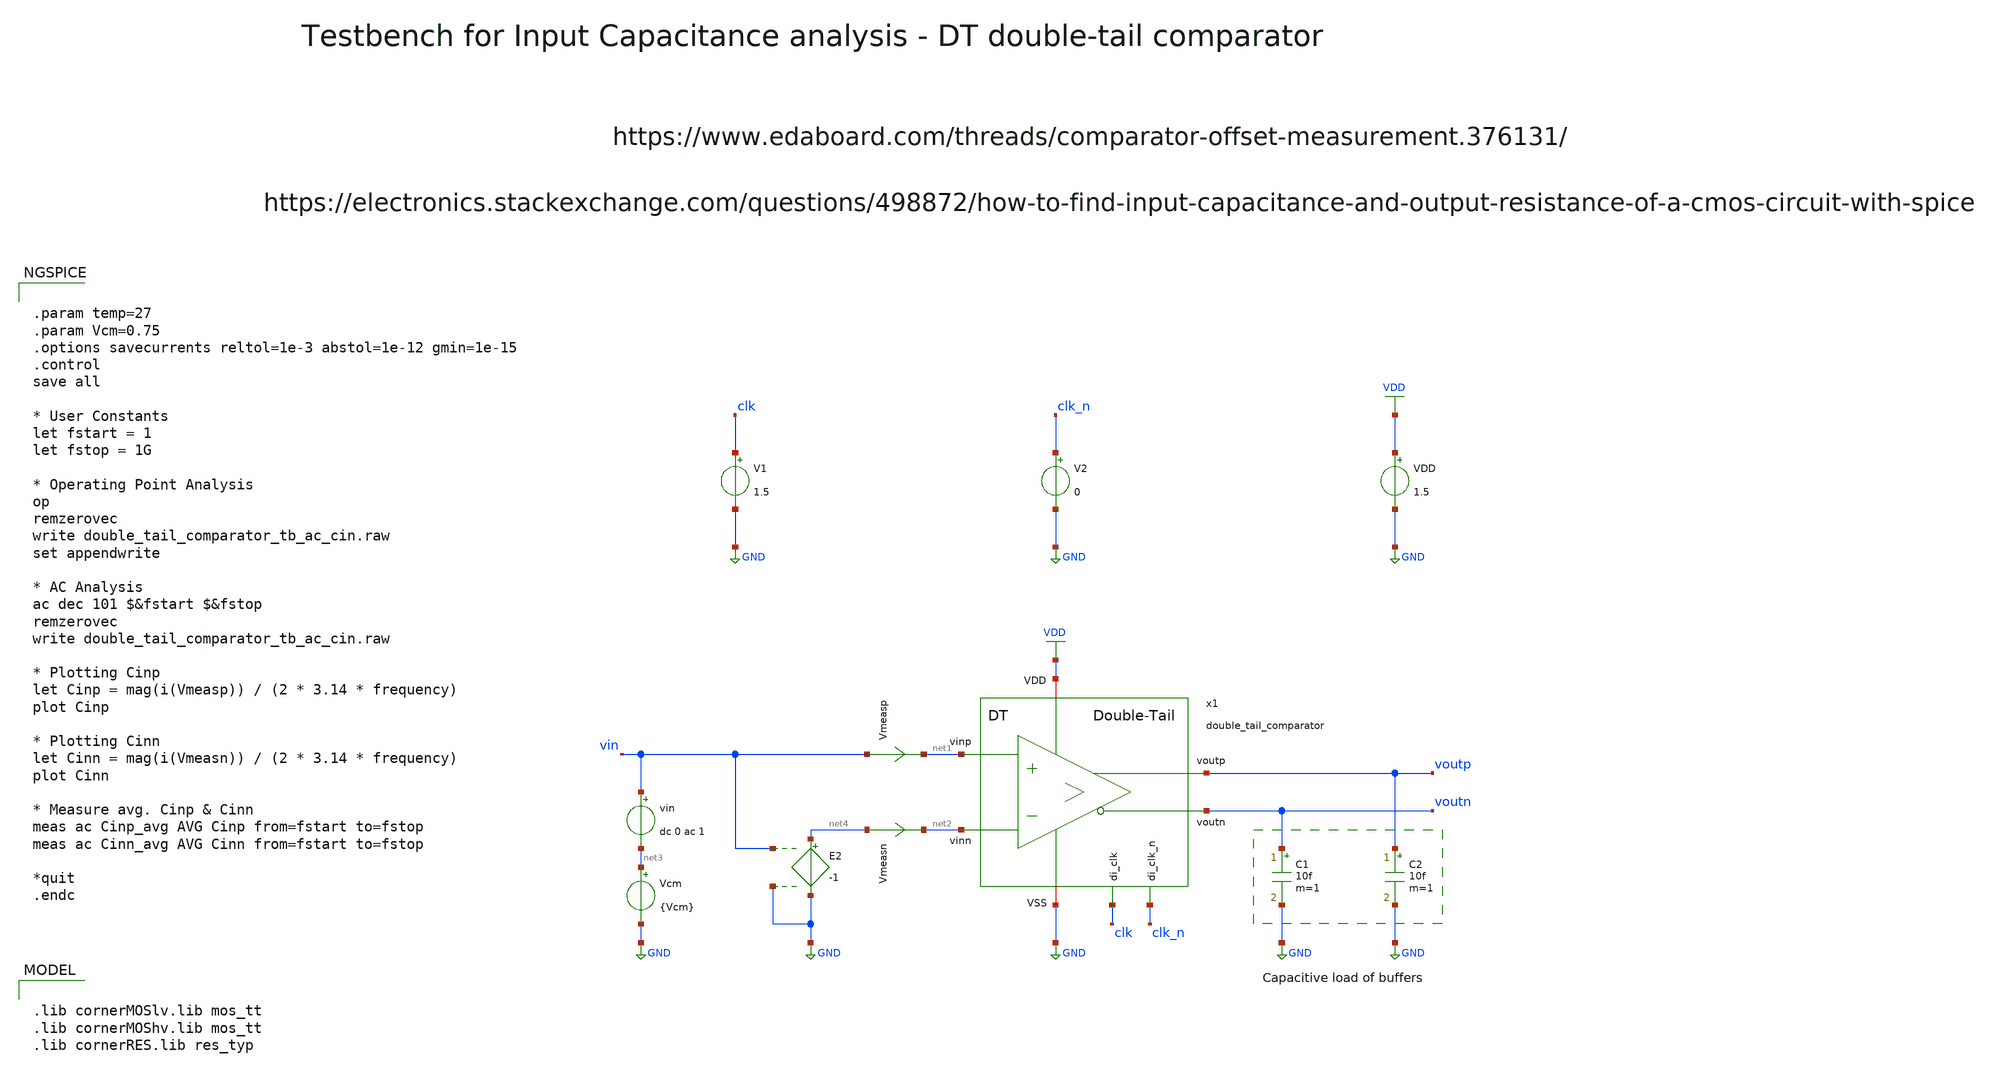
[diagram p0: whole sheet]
** sch_path: SG13G2_ATBS-ADC-main/xschem/comparator/discrete_time/Double-tail/testbenches/double_tail_comparator_tb_ac_cin.sch
**.subckt double_tail_comparator_tb_ac_cin
VDD VDD GND 1.5
V1 clk GND 1.5
V2 clk_n GND 0
C1 voutn GND 10f m=1
C2 voutp GND 10f m=1
Vmeasp vin net1 0
.save i(vmeasp)
Vmeasn net4 net2 0
.save i(vmeasn)
vin vin net3 dc 0 ac 1
Vcm net3 GND {Vcm}
E2 net4 GND vin GND -1
x1 clk_n clk VDD voutp net1 GND voutn net2 double_tail_comparator
**** begin user architecture code

.lib cornerMOSlv.lib mos_tt
.lib cornerMOShv.lib mos_tt
.lib cornerRES.lib res_typ



.param temp=27
.param Vcm=0.75
.options savecurrents reltol=1e-3 abstol=1e-12 gmin=1e-15
.control
save all

* User Constants
let fstart = 1
let fstop = 1G

* Operating Point Analysis
op
remzerovec
write double_tail_comparator_tb_ac_cin.raw
set appendwrite

* AC Analysis
ac dec 101 $&fstart $&fstop
remzerovec
write double_tail_comparator_tb_ac_cin.raw

* Plotting Cinp
let Cinp = mag(i(Vmeasp)) / (2 * 3.14 * frequency)
plot Cinp

* Plotting Cinn
let Cinn = mag(i(Vmeasn)) / (2 * 3.14 * frequency)
plot Cinn

* Measure avg. Cinp & Cinn
meas ac Cinp_avg AVG Cinp from=fstart to=fstop
meas ac Cinn_avg AVG Cinn from=fstart to=fstop

*quit
.endc

**** end user architecture code
**.ends

* expanding   symbol:  comparator/discrete_time/Double-tail/double_tail_comparator.sym # of pins=8
** sym_path: SG13G2_ATBS-ADC-main/xschem/comparator/discrete_time/Double-tail/double_tail_comparator.sym
** sch_path: SG13G2_ATBS-ADC-main/xschem/comparator/discrete_time/Double-tail/double_tail_comparator.sch
.subckt double_tail_comparator di_clk_n di_clk VDD voutp vinp VSS voutn vinn
*.opin voutp
*.opin voutn
*.ipin di_clk_n
*.iopin VDD
*.iopin VSS
*.ipin vinp
*.ipin vinn
*.ipin di_clk
XM6 voutp vcpn VSS VSS sg13_lv_nmos w=1.0u l=0.13u ng=1 m=1 mm_ok=1
XM8 net1 di_clk_n VDD VDD sg13_lv_pmos w=2.0u l=0.13u ng=2 m=1 mm_ok=1
XM9 voutp voutn net1 VDD sg13_lv_pmos w=2.0u l=0.13u ng=2 m=1 mm_ok=1
XM10 voutn voutp net1 VDD sg13_lv_pmos w=2.0u l=0.13u ng=2 m=1 mm_ok=1
XM11 voutp voutn VSS VSS sg13_lv_nmos w=1.0u l=0.13u ng=1 m=1 mm_ok=1
XM12 voutn voutp VSS VSS sg13_lv_nmos w=1.0u l=0.13u ng=1 m=1 mm_ok=1
XM7 voutn vcpp VSS VSS sg13_lv_nmos w=1.0u l=0.13u ng=1 m=1 mm_ok=1
CP1 vcpn VSS 300f m=1
CP2 vcpp VSS 300f m=1
XM1 vcpn vinp vs VSS sg13_lv_nmos w=1.0u l=0.13u ng=1 m=1 mm_ok=1
XM2 vcpp vinn vs VSS sg13_lv_nmos w=1.0u l=0.13u ng=1 m=1 mm_ok=1
XM3 vs di_clk VSS VSS sg13_lv_nmos w=1.0u l=0.13u ng=1 m=1 mm_ok=1
XM4 vcpn di_clk VDD VDD sg13_lv_pmos w=1.0u l=0.13u ng=1 m=1 mm_ok=1
XM5 vcpp di_clk VDD VDD sg13_lv_pmos w=1.0u l=0.13u ng=1 m=1 mm_ok=1
.ends

.GLOBAL GND
.GLOBAL VDD
.end
